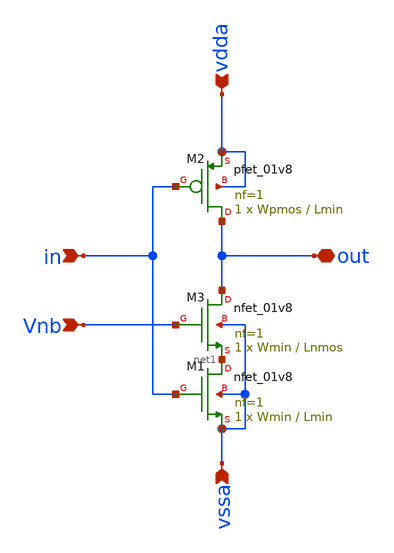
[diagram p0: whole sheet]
** sch_path: xschem/inv/inv_weak_pulldown.sch
**.subckt inv_weak_pulldown in out Vnb vdda vssa
*.ipin in
*.iopin out
*.ipin Vnb
*.ipin vdda
*.ipin vssa
XM1 net1 in vssa vssa sky130_fd_pr__nfet_01v8 L=Lmin W=Wmin nf=1 ad='int((nf+1)/2) * W/nf * 0.29' as='int((nf+2)/2) * W/nf * 0.29'
+ pd='2*int((nf+1)/2) * (W/nf + 0.29)' ps='2*int((nf+2)/2) * (W/nf + 0.29)' nrd='0.29 / W' nrs='0.29 / W'
+ sa=0 sb=0 sd=0 mult=1 m=1
XM2 out in vdda vdda sky130_fd_pr__pfet_01v8 L=Lmin W=Wpmos nf=1 ad='int((nf+1)/2) * W/nf * 0.29' as='int((nf+2)/2) * W/nf * 0.29'
+ pd='2*int((nf+1)/2) * (W/nf + 0.29)' ps='2*int((nf+2)/2) * (W/nf + 0.29)' nrd='0.29 / W' nrs='0.29 / W'
+ sa=0 sb=0 sd=0 mult=1 m=1
XM3 out Vnb net1 vssa sky130_fd_pr__nfet_01v8 L=Lnmos W=Wmin nf=1 ad='int((nf+1)/2) * W/nf * 0.29' as='int((nf+2)/2) * W/nf * 0.29'
+ pd='2*int((nf+1)/2) * (W/nf + 0.29)' ps='2*int((nf+2)/2) * (W/nf + 0.29)' nrd='0.29 / W' nrs='0.29 / W'
+ sa=0 sb=0 sd=0 mult=1 m=1
**.ends
.end
